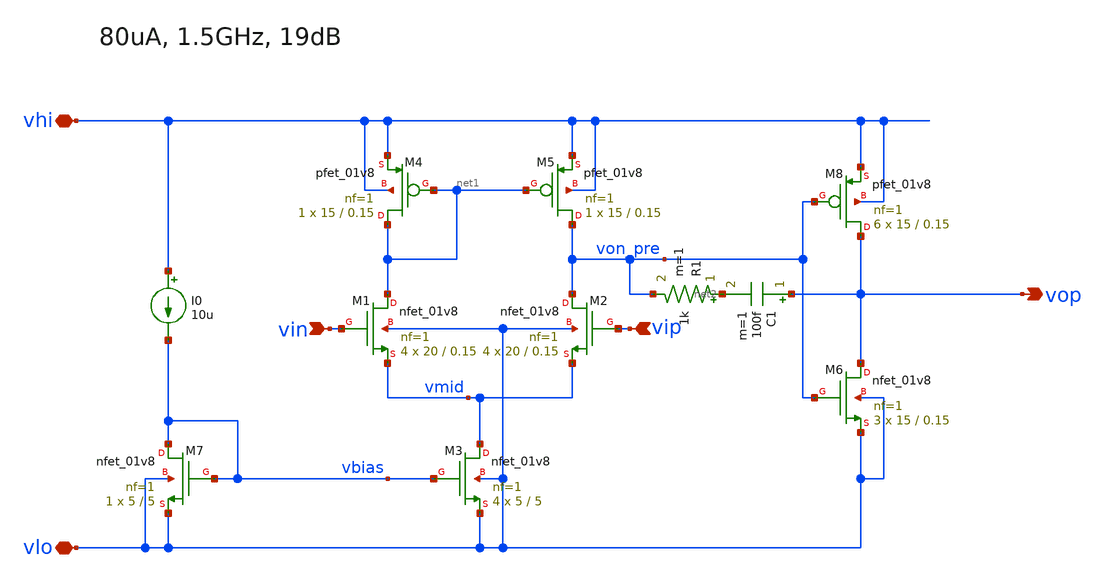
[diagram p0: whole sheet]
** sch_path: xschem/5tamp_model.sch
**.subckt 5tamp_model vip vin vop vhi vlo
*.ipin vip
*.ipin vin
*.opin vop
*.iopin vhi
*.iopin vlo
XM1 net1 vin vmid vlo sky130_fd_pr__nfet_01v8 L=0.15 W=20 nf=1 ad='int((nf+1)/2) * W/nf * 0.29' as='int((nf+2)/2) * W/nf * 0.29'
+ pd='2*int((nf+1)/2) * (W/nf + 0.29)' ps='2*int((nf+2)/2) * (W/nf + 0.29)' nrd='0.29 / W' nrs='0.29 / W'
+ sa=0 sb=0 sd=0 mult=4 m=4
XM2 von_pre vip vmid vlo sky130_fd_pr__nfet_01v8 L=0.15 W=20 nf=1 ad='int((nf+1)/2) * W/nf * 0.29' as='int((nf+2)/2) * W/nf * 0.29'
+ pd='2*int((nf+1)/2) * (W/nf + 0.29)' ps='2*int((nf+2)/2) * (W/nf + 0.29)' nrd='0.29 / W' nrs='0.29 / W'
+ sa=0 sb=0 sd=0 mult=4 m=4
XM3 vmid vbias vlo vlo sky130_fd_pr__nfet_01v8 L=5 W=5 nf=1 ad='int((nf+1)/2) * W/nf * 0.29' as='int((nf+2)/2) * W/nf * 0.29'
+ pd='2*int((nf+1)/2) * (W/nf + 0.29)' ps='2*int((nf+2)/2) * (W/nf + 0.29)' nrd='0.29 / W' nrs='0.29 / W'
+ sa=0 sb=0 sd=0 mult=4 m=4
XM4 net1 net1 vhi vhi sky130_fd_pr__pfet_01v8 L=0.15 W=15 nf=1 ad='int((nf+1)/2) * W/nf * 0.29' as='int((nf+2)/2) * W/nf * 0.29'
+ pd='2*int((nf+1)/2) * (W/nf + 0.29)' ps='2*int((nf+2)/2) * (W/nf + 0.29)' nrd='0.29 / W' nrs='0.29 / W'
+ sa=0 sb=0 sd=0 mult=1 m=1
XM5 von_pre net1 vhi vhi sky130_fd_pr__pfet_01v8 L=0.15 W=15 nf=1 ad='int((nf+1)/2) * W/nf * 0.29' as='int((nf+2)/2) * W/nf * 0.29'
+ pd='2*int((nf+1)/2) * (W/nf + 0.29)' ps='2*int((nf+2)/2) * (W/nf + 0.29)' nrd='0.29 / W' nrs='0.29 / W'
+ sa=0 sb=0 sd=0 mult=1 m=1
I0 vhi vbias 10u
XM7 vbias vbias vlo vlo sky130_fd_pr__nfet_01v8 L=5 W=5 nf=1 ad='int((nf+1)/2) * W/nf * 0.29' as='int((nf+2)/2) * W/nf * 0.29'
+ pd='2*int((nf+1)/2) * (W/nf + 0.29)' ps='2*int((nf+2)/2) * (W/nf + 0.29)' nrd='0.29 / W' nrs='0.29 / W'
+ sa=0 sb=0 sd=0 mult=1 m=1
XM6 vop von_pre vlo vlo sky130_fd_pr__nfet_01v8 L=0.15 W=15 nf=1 ad='int((nf+1)/2) * W/nf * 0.29' as='int((nf+2)/2) * W/nf * 0.29'
+ pd='2*int((nf+1)/2) * (W/nf + 0.29)' ps='2*int((nf+2)/2) * (W/nf + 0.29)' nrd='0.29 / W' nrs='0.29 / W'
+ sa=0 sb=0 sd=0 mult=3 m=3
XM8 vop von_pre vhi vhi sky130_fd_pr__pfet_01v8 L=0.15 W=15 nf=1 ad='int((nf+1)/2) * W/nf * 0.29' as='int((nf+2)/2) * W/nf * 0.29'
+ pd='2*int((nf+1)/2) * (W/nf + 0.29)' ps='2*int((nf+2)/2) * (W/nf + 0.29)' nrd='0.29 / W' nrs='0.29 / W'
+ sa=0 sb=0 sd=0 mult=6 m=6
C1 vop net2 100f m=1
R1 net2 von_pre 1k m=1
**.ends
.end
